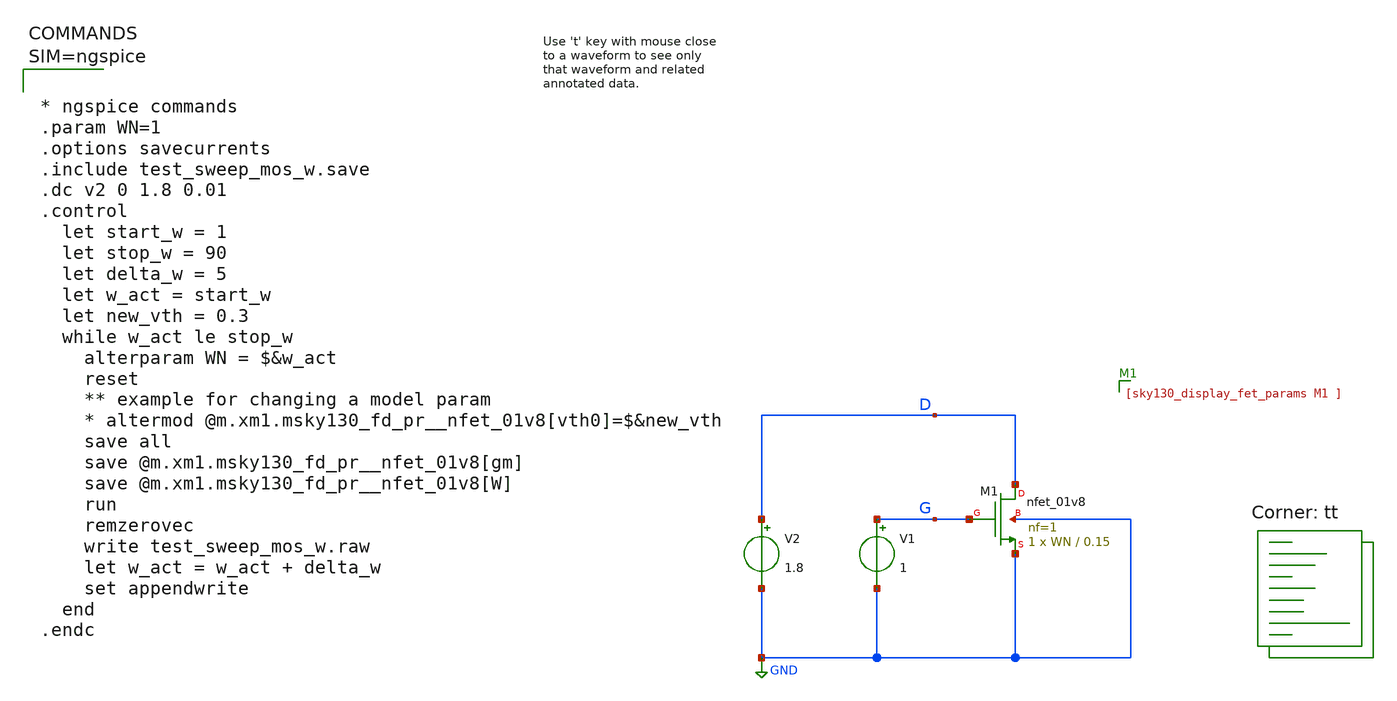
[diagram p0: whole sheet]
** sch_path: sky130A/xschem_libs/sky130_tests/test_sweep_mos_w/schematic/test_sweep_mos_w.sch
* Copyright 2021 Stefan Frederik Schippers
* Licensed under the Apache License, Version 2.0 (the "License");
* you may not use this file except in compliance with the License.
* You may obtain a copy of the License at
* https://www.apache.org/licenses/LICENSE-2.0
* Unless required by applicable law or agreed to in writing, software
* distributed under the License is distributed on an "AS IS" BASIS,
* WITHOUT WARRANTIES OR CONDITIONS OF ANY KIND, either express or implied.
* See the License for the specific language governing permissions and
* limitations under the License.
**.subckt test_sweep_mos_w
V1 G GND 1
V2 D GND 1.8
XM1 D G GND GND sky130_fd_pr__nfet_01v8 L=0.15 W=WN nf=1 ad='int((1 + 1)/2) * WN / 1 * 0.29' as='int((1 + 2)/2) * WN / 1 * 0.29'
+ pd='2*int((1 + 1)/2) * (WN / 1 + 0.29)' ps='2*int((1 + 2)/2) * (WN / 1 + 0.29)' nrd='0.29 / WN ' nrs='0.29 / WN '
+ sa=0 sb=0 sd=0 mult=1 m=1
**** begin user architecture code
.lib $::SKYWATER_MODELS/sky130.lib.spice tt



* ngspice commands
.param WN=1
.options savecurrents
.include test_sweep_mos_w.save
.dc v2 0 1.8 0.01
.control
  let start_w = 1
  let stop_w = 90
  let delta_w = 5
  let w_act = start_w
  let new_vth = 0.3
  while w_act le stop_w
    alterparam WN = $&w_act
    reset
    ** example for changing a model param
    * altermod @m.xm1.msky130_fd_pr__nfet_01v8[vth0]=$&new_vth
    save all
    save @m.xm1.msky130_fd_pr__nfet_01v8[gm]
    save @m.xm1.msky130_fd_pr__nfet_01v8[W]
    run
    remzerovec
    write test_sweep_mos_w.raw
    let w_act = w_act + delta_w
    set appendwrite
  end
.endc



**** end user architecture code
**.ends
.GLOBAL GND
.end
